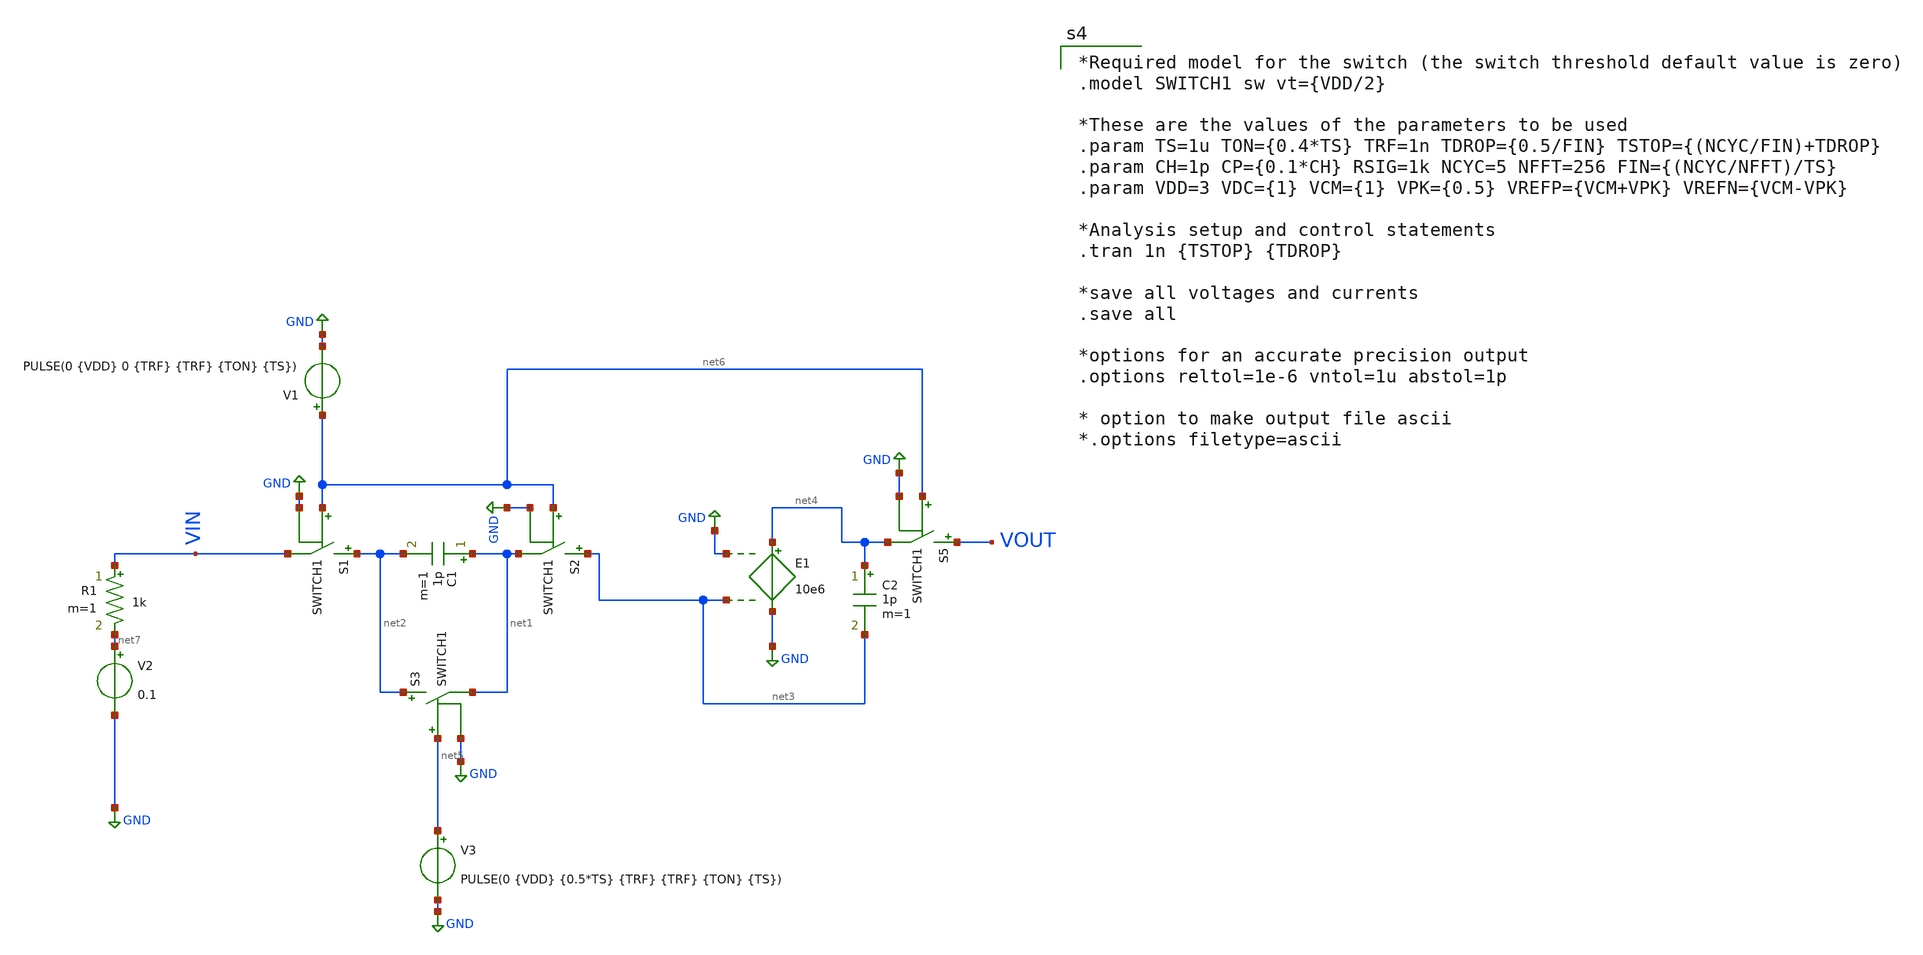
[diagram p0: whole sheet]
** sch_path: SC_example.sch
**.subckt SC_example
S1 net2 VIN net6 GND SWITCH1
S2 net3 net1 net6 GND SWITCH1
C1 net1 net2 1p m=1
S3 net2 net1 net5 GND SWITCH1
E1 net4 GND GND net3 10e6
C2 net4 net3 1p m=1
V3 net5 GND PULSE(0 {VDD} {0.5*TS} {TRF} {TRF} {TON} {TS})
V1 net6 GND PULSE(0 {VDD} 0 {TRF} {TRF} {TON} {TS})
V2 net7 GND 0.1
S5 VOUT net4 net6 GND SWITCH1
R1 VIN net7 1k m=1
**** begin user architecture code

*Required model for the switch (the switch threshold default value is zero)
.model SWITCH1 sw vt={VDD/2}

*These are the values of the parameters to be used
.param TS=1u TON={0.4*TS} TRF=1n TDROP={0.5/FIN} TSTOP={(NCYC/FIN)+TDROP}
.param CH=1p CP={0.1*CH} RSIG=1k NCYC=5 NFFT=256 FIN={(NCYC/NFFT)/TS}
.param VDD=3 VDC={1} VCM={1} VPK={0.5} VREFP={VCM+VPK} VREFN={VCM-VPK}

*Analysis setup and control statements
.tran 1n {TSTOP} {TDROP}

*save all voltages and currents
.save all

*options for an accurate precision output
.options reltol=1e-6 vntol=1u abstol=1p

* option to make output file ascii
*.options filetype=ascii




**** end user architecture code
**.ends
.GLOBAL GND
.end
